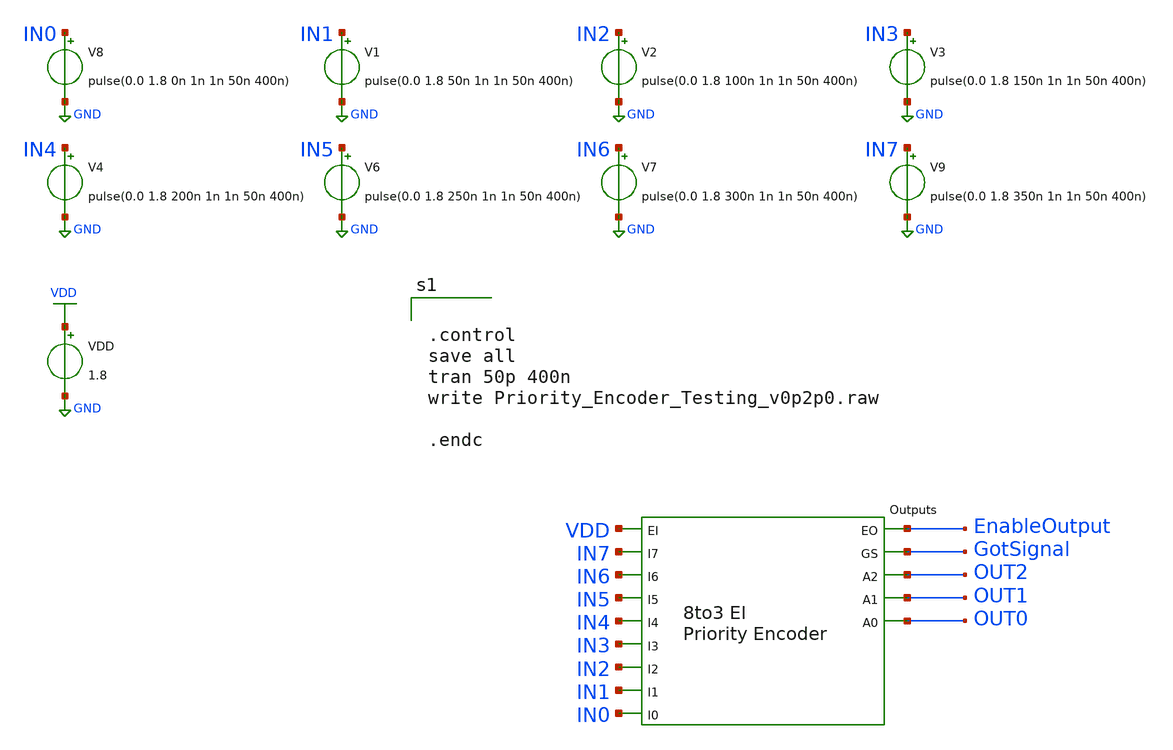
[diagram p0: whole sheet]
** sch_path: PriorityEncoder/xschem/Priority_Encoder_Testing_v0p2p1.sch
.lib $::SKYWATER_MODELS/sky130.lib.spice tt
.include $::SKYWATER_STDCELLS/sky130_fd_sc_hd.spice

**.subckt Priority_Encoder_Testing_v0p2p1
VDD VDD GND 1.8
x1 IN1 IN5 IN3 IN0 IN2 IN6 IN7 IN4 EnableOutput GotSignal OUT2 OUT1 OUT0 VDD
+ 8to3_Priority_Encoder_v0p2p0
V8 IN0 GND pulse(0.0 1.8 0n 1n 1n 50n 400n)
V1 IN1 GND pulse(0.0 1.8 50n 1n 1n 50n 400n)
V2 IN2 GND pulse(0.0 1.8 100n 1n 1n 50n 400n)
V3 IN3 GND pulse(0.0 1.8 150n 1n 1n 50n 400n)
V4 IN4 GND pulse(0.0 1.8 200n 1n 1n 50n 400n)
V6 IN5 GND pulse(0.0 1.8 250n 1n 1n 50n 400n)
V7 IN6 GND pulse(0.0 1.8 300n 1n 1n 50n 400n)
V9 IN7 GND pulse(0.0 1.8 350n 1n 1n 50n 400n)
**** begin user architecture code


.control
save all
tran 50p 400n
write Priority_Encoder_Testing_v0p2p0.raw

.endc


**** end user architecture code
**.ends
.GLOBAL GND
.GLOBAL VDD
.end
